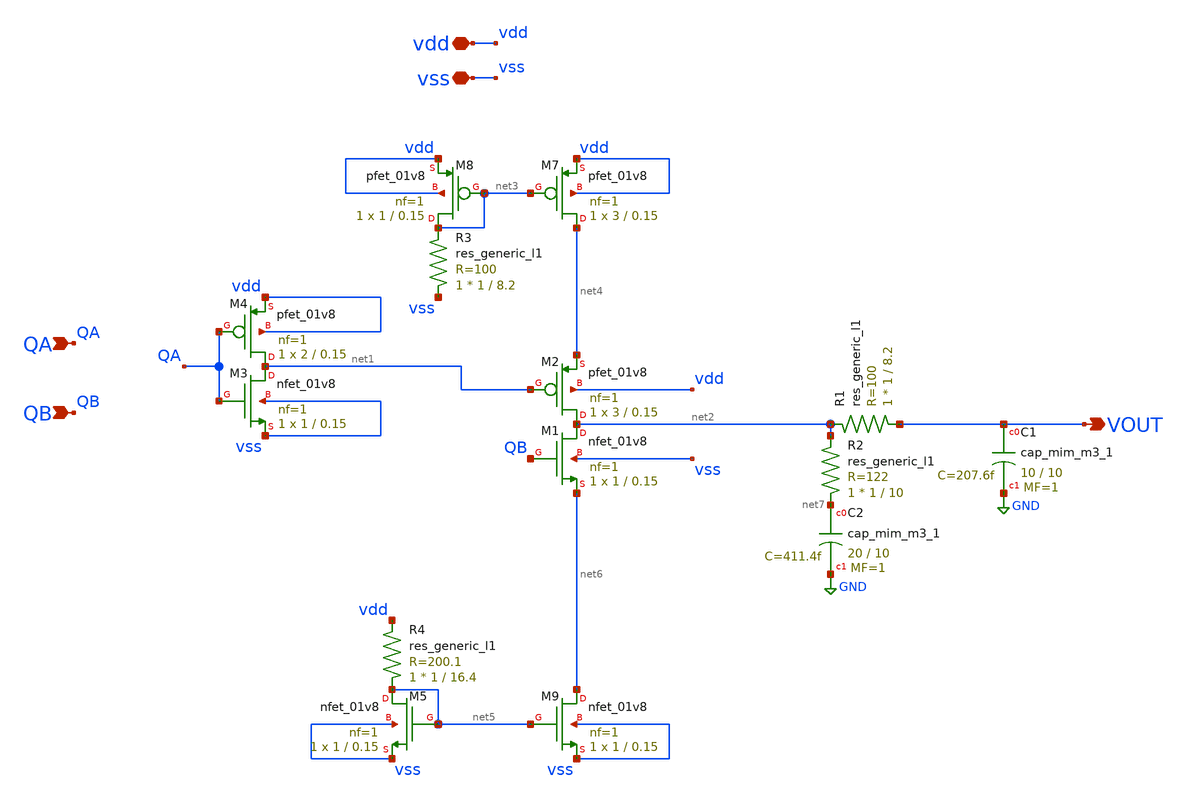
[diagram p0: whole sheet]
** sch_path: xschem/charge_pump.sch
**.subckt charge_pump vdd vss QA VOUT QB
*.iopin vdd
*.iopin vss
*.ipin QA
*.opin VOUT
*.ipin QB
XM1 net2 QB net6 vss sky130_fd_pr__nfet_01v8 L=0.15 W=1 nf=1 ad='int((nf+1)/2) * W/nf * 0.29' as='int((nf+2)/2) * W/nf * 0.29'
+ pd='2*int((nf+1)/2) * (W/nf + 0.29)' ps='2*int((nf+2)/2) * (W/nf + 0.29)' nrd='0.29 / W' nrs='0.29 / W'
+ sa=0 sb=0 sd=0 mult=1 m=1
XM2 net2 net1 net4 vdd sky130_fd_pr__pfet_01v8 L=0.15 W=3 nf=1 ad='int((nf+1)/2) * W/nf * 0.29' as='int((nf+2)/2) * W/nf * 0.29'
+ pd='2*int((nf+1)/2) * (W/nf + 0.29)' ps='2*int((nf+2)/2) * (W/nf + 0.29)' nrd='0.29 / W' nrs='0.29 / W'
+ sa=0 sb=0 sd=0 mult=1 m=1
XM3 net1 QA vss vss sky130_fd_pr__nfet_01v8 L=0.15 W=1 nf=1 ad='int((nf+1)/2) * W/nf * 0.29' as='int((nf+2)/2) * W/nf * 0.29'
+ pd='2*int((nf+1)/2) * (W/nf + 0.29)' ps='2*int((nf+2)/2) * (W/nf + 0.29)' nrd='0.29 / W' nrs='0.29 / W'
+ sa=0 sb=0 sd=0 mult=1 m=1
XM4 net1 QA vdd vdd sky130_fd_pr__pfet_01v8 L=0.15 W=2 nf=1 ad='int((nf+1)/2) * W/nf * 0.29' as='int((nf+2)/2) * W/nf * 0.29'
+ pd='2*int((nf+1)/2) * (W/nf + 0.29)' ps='2*int((nf+2)/2) * (W/nf + 0.29)' nrd='0.29 / W' nrs='0.29 / W'
+ sa=0 sb=0 sd=0 mult=1 m=1
XC2 net7 GND sky130_fd_pr__cap_mim_m3_1 W=20 L=10 MF=1 m=1
R2 net7 net2 sky130_fd_pr__res_generic_l1 W=1 L=10 m=1
XC1 VOUT GND sky130_fd_pr__cap_mim_m3_1 W=10 L=10 MF=1 m=1
XM7 net4 net3 vdd vdd sky130_fd_pr__pfet_01v8 L=0.15 W=3 nf=1 ad='int((nf+1)/2) * W/nf * 0.29' as='int((nf+2)/2) * W/nf * 0.29'
+ pd='2*int((nf+1)/2) * (W/nf + 0.29)' ps='2*int((nf+2)/2) * (W/nf + 0.29)' nrd='0.29 / W' nrs='0.29 / W'
+ sa=0 sb=0 sd=0 mult=1 m=1
XM8 net3 net3 vdd vdd sky130_fd_pr__pfet_01v8 L=0.15 W=1 nf=1 ad='int((nf+1)/2) * W/nf * 0.29' as='int((nf+2)/2) * W/nf * 0.29'
+ pd='2*int((nf+1)/2) * (W/nf + 0.29)' ps='2*int((nf+2)/2) * (W/nf + 0.29)' nrd='0.29 / W' nrs='0.29 / W'
+ sa=0 sb=0 sd=0 mult=1 m=1
XM9 net6 net5 vss vss sky130_fd_pr__nfet_01v8 L=0.15 W=1 nf=1 ad='int((nf+1)/2) * W/nf * 0.29' as='int((nf+2)/2) * W/nf * 0.29'
+ pd='2*int((nf+1)/2) * (W/nf + 0.29)' ps='2*int((nf+2)/2) * (W/nf + 0.29)' nrd='0.29 / W' nrs='0.29 / W'
+ sa=0 sb=0 sd=0 mult=1 m=1
XM5 net5 net5 vss vss sky130_fd_pr__nfet_01v8 L=0.15 W=1 nf=1 ad='int((nf+1)/2) * W/nf * 0.29' as='int((nf+2)/2) * W/nf * 0.29'
+ pd='2*int((nf+1)/2) * (W/nf + 0.29)' ps='2*int((nf+2)/2) * (W/nf + 0.29)' nrd='0.29 / W' nrs='0.29 / W'
+ sa=0 sb=0 sd=0 mult=1 m=1
R3 vss net3 sky130_fd_pr__res_generic_l1 W=1 L=8.2 m=1
R4 net5 vdd sky130_fd_pr__res_generic_l1 W=1 L=16.4 m=1
R1 VOUT net2 sky130_fd_pr__res_generic_l1 W=1 L=8.2 m=1
**.ends
.GLOBAL GND
.end
